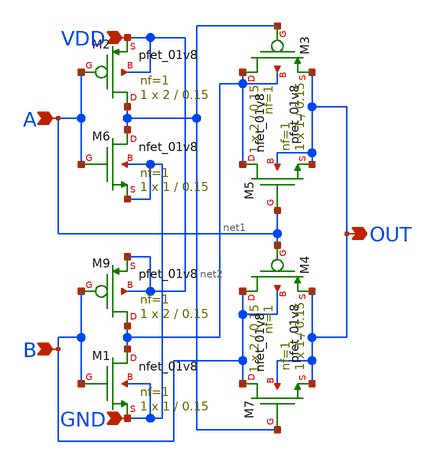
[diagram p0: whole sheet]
** sch_path: sch/XOR.sch
**.subckt XOR A B VDD GND OUT
*.ipin A
*.ipin B
*.ipin VDD
*.ipin GND
*.opin OUT
XM1 net1 B GND GND sky130_fd_pr__nfet_01v8 L=0.15 W=1 nf=1 ad='int((1 + 1)/2) * 1 / 1 * 0.29' as='int((1 + 2)/2) * 1 / 1 * 0.29'
+ pd='2*int((1 + 1)/2) * (1 / 1 + 0.29)' ps='2*int((1 + 2)/2) * (1 / 1 + 0.29)' nrd='0.29 / 1 ' nrs='0.29 / 1 '
+ sa=0 sb=0 sd=0 mult=1 m=1
XM2 net2 A VDD VDD sky130_fd_pr__pfet_01v8 L=0.15 W=2 nf=1 ad='int((1 + 1)/2) * 2 / 1 * 0.29' as='int((1 + 2)/2) * 2 / 1 * 0.29'
+ pd='2*int((1 + 1)/2) * (2 / 1 + 0.29)' ps='2*int((1 + 2)/2) * (2 / 1 + 0.29)' nrd='0.29 / 2 ' nrs='0.29 / 2 '
+ sa=0 sb=0 sd=0 mult=1 m=1
XM3 net1 net2 OUT net1 sky130_fd_pr__pfet_01v8 L=0.15 W=2 nf=1 ad='int((1 + 1)/2) * 2 / 1 * 0.29' as='int((1 + 2)/2) * 2 / 1 * 0.29'
+ pd='2*int((1 + 1)/2) * (2 / 1 + 0.29)' ps='2*int((1 + 2)/2) * (2 / 1 + 0.29)' nrd='0.29 / 2 ' nrs='0.29 / 2 '
+ sa=0 sb=0 sd=0 mult=1 m=1
XM4 B A OUT B sky130_fd_pr__pfet_01v8 L=0.15 W=2 nf=1 ad='int((1 + 1)/2) * 2 / 1 * 0.29' as='int((1 + 2)/2) * 2 / 1 * 0.29'
+ pd='2*int((1 + 1)/2) * (2 / 1 + 0.29)' ps='2*int((1 + 2)/2) * (2 / 1 + 0.29)' nrd='0.29 / 2 ' nrs='0.29 / 2 '
+ sa=0 sb=0 sd=0 mult=1 m=1
XM5 net1 A OUT OUT sky130_fd_pr__nfet_01v8 L=0.15 W=1 nf=1 ad='int((1 + 1)/2) * 1 / 1 * 0.29' as='int((1 + 2)/2) * 1 / 1 * 0.29'
+ pd='2*int((1 + 1)/2) * (1 / 1 + 0.29)' ps='2*int((1 + 2)/2) * (1 / 1 + 0.29)' nrd='0.29 / 1 ' nrs='0.29 / 1 '
+ sa=0 sb=0 sd=0 mult=1 m=1
XM7 B net2 OUT OUT sky130_fd_pr__nfet_01v8 L=0.15 W=1 nf=1 ad='int((1 + 1)/2) * 1 / 1 * 0.29' as='int((1 + 2)/2) * 1 / 1 * 0.29'
+ pd='2*int((1 + 1)/2) * (1 / 1 + 0.29)' ps='2*int((1 + 2)/2) * (1 / 1 + 0.29)' nrd='0.29 / 1 ' nrs='0.29 / 1 '
+ sa=0 sb=0 sd=0 mult=1 m=1
XM6 net2 A GND GND sky130_fd_pr__nfet_01v8 L=0.15 W=1 nf=1 ad='int((1 + 1)/2) * 1 / 1 * 0.29' as='int((1 + 2)/2) * 1 / 1 * 0.29'
+ pd='2*int((1 + 1)/2) * (1 / 1 + 0.29)' ps='2*int((1 + 2)/2) * (1 / 1 + 0.29)' nrd='0.29 / 1 ' nrs='0.29 / 1 '
+ sa=0 sb=0 sd=0 mult=1 m=1
XM9 net1 B VDD VDD sky130_fd_pr__pfet_01v8 L=0.15 W=2 nf=1 ad='int((1 + 1)/2) * 2 / 1 * 0.29' as='int((1 + 2)/2) * 2 / 1 * 0.29'
+ pd='2*int((1 + 1)/2) * (2 / 1 + 0.29)' ps='2*int((1 + 2)/2) * (2 / 1 + 0.29)' nrd='0.29 / 2 ' nrs='0.29 / 2 '
+ sa=0 sb=0 sd=0 mult=1 m=1
**.ends
.end
